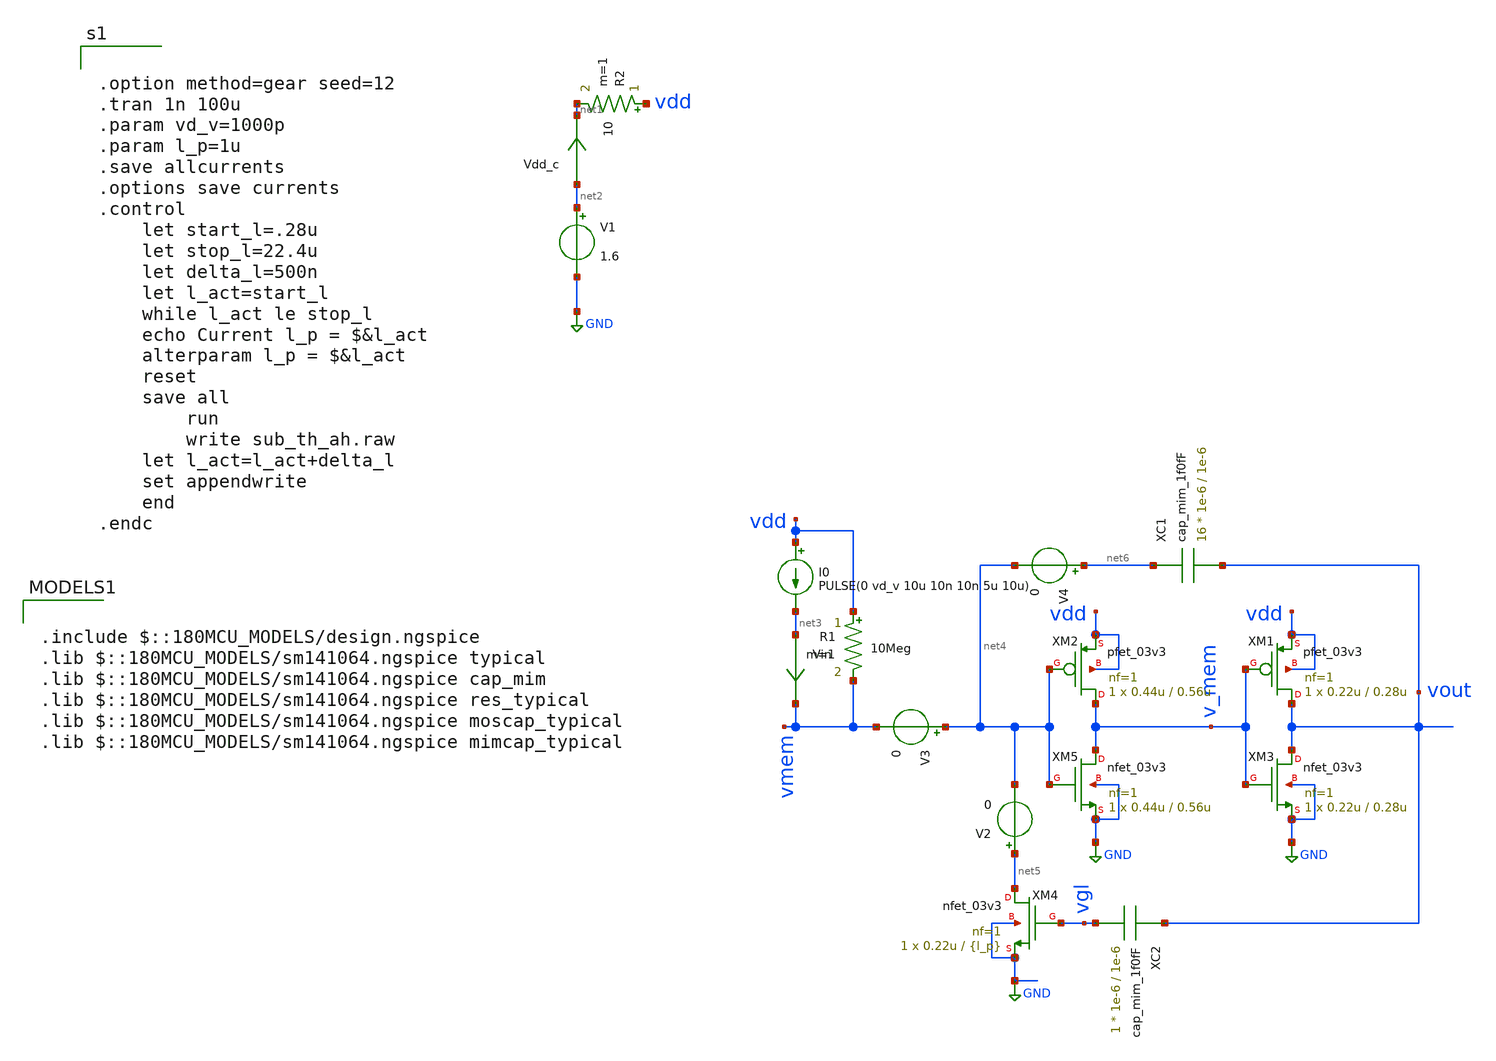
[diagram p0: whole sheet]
** sch_path: miscellaneous/AH_neuron_size.sch
**.subckt AH_neuron_size
V1 net2 GND 1.6
Vdd_c net2 net1 0
.save i(vdd_c)
Vin net3 vmem 0
.save i(vin)
XC1 net6 vout cap_mim_1f0fF c_width=1e-6 c_length=1e-6 m=16
XC2 vout vgl cap_mim_1f0fF c_width=1e-6 c_length=1e-6 m=1
XM4 net5 vgl GND GND nfet_03v3 L={l_p} W=0.22u nf=1 ad='int((nf+1)/2) * W/nf * 0.18u' as='int((nf+2)/2) * W/nf * 0.18u'
+ pd='2*int((nf+1)/2) * (W/nf + 0.18u)' ps='2*int((nf+2)/2) * (W/nf + 0.18u)' nrd='0.18u / W' nrs='0.18u / W'
+ sa=0 sb=0 sd=0 m=1
V2 net5 net4 0
V3 net4 vmem 0
V4 net6 net4 0
I0 vdd net3 PULSE(0 vd_v 10u 10n 10n 5u 10u)
R1 vdd vmem 10Meg m=1
R2 vdd net1 10 m=1
XM2 v_mem net4 vdd vdd pfet_03v3 L=0.56u W=0.44u nf=1 ad='int((nf+1)/2) * W/nf * 0.18u' as='int((nf+2)/2) * W/nf * 0.18u'
+ pd='2*int((nf+1)/2) * (W/nf + 0.18u)' ps='2*int((nf+2)/2) * (W/nf + 0.18u)' nrd='0.18u / W' nrs='0.18u / W'
+ sa=0 sb=0 sd=0 m=1
XM5 v_mem net4 GND GND nfet_03v3 L=0.56u W=0.44u nf=1 ad='int((nf+1)/2) * W/nf * 0.18u' as='int((nf+2)/2) * W/nf * 0.18u'
+ pd='2*int((nf+1)/2) * (W/nf + 0.18u)' ps='2*int((nf+2)/2) * (W/nf + 0.18u)' nrd='0.18u / W' nrs='0.18u / W'
+ sa=0 sb=0 sd=0 m=1
XM1 vout v_mem vdd vdd pfet_03v3 L=0.28u W=0.22u nf=1 ad='int((nf+1)/2) * W/nf * 0.18u' as='int((nf+2)/2) * W/nf * 0.18u'
+ pd='2*int((nf+1)/2) * (W/nf + 0.18u)' ps='2*int((nf+2)/2) * (W/nf + 0.18u)' nrd='0.18u / W' nrs='0.18u / W'
+ sa=0 sb=0 sd=0 m=1
XM3 vout v_mem GND GND nfet_03v3 L=0.28u W=0.22u nf=1 ad='int((nf+1)/2) * W/nf * 0.18u' as='int((nf+2)/2) * W/nf * 0.18u'
+ pd='2*int((nf+1)/2) * (W/nf + 0.18u)' ps='2*int((nf+2)/2) * (W/nf + 0.18u)' nrd='0.18u / W' nrs='0.18u / W'
+ sa=0 sb=0 sd=0 m=1
**** begin user architecture code


.option method=gear seed=12
.tran 1n 100u
.param vd_v=1000p
.param l_p=1u
.save allcurrents
.options save currents
.control
    let start_l=.28u
    let stop_l=22.4u
    let delta_l=500n
    let l_act=start_l
    while l_act le stop_l
	echo Current l_p = $&l_act
	alterparam l_p = $&l_act
	reset
	save all
        run
        write sub_th_ah.raw
	let l_act=l_act+delta_l
	set appendwrite
    end
.endc



.include $::180MCU_MODELS/design.ngspice
.lib $::180MCU_MODELS/sm141064.ngspice typical
.lib $::180MCU_MODELS/sm141064.ngspice cap_mim
.lib $::180MCU_MODELS/sm141064.ngspice res_typical
.lib $::180MCU_MODELS/sm141064.ngspice moscap_typical
.lib $::180MCU_MODELS/sm141064.ngspice mimcap_typical

**** end user architecture code
**.ends
.GLOBAL GND
.end
